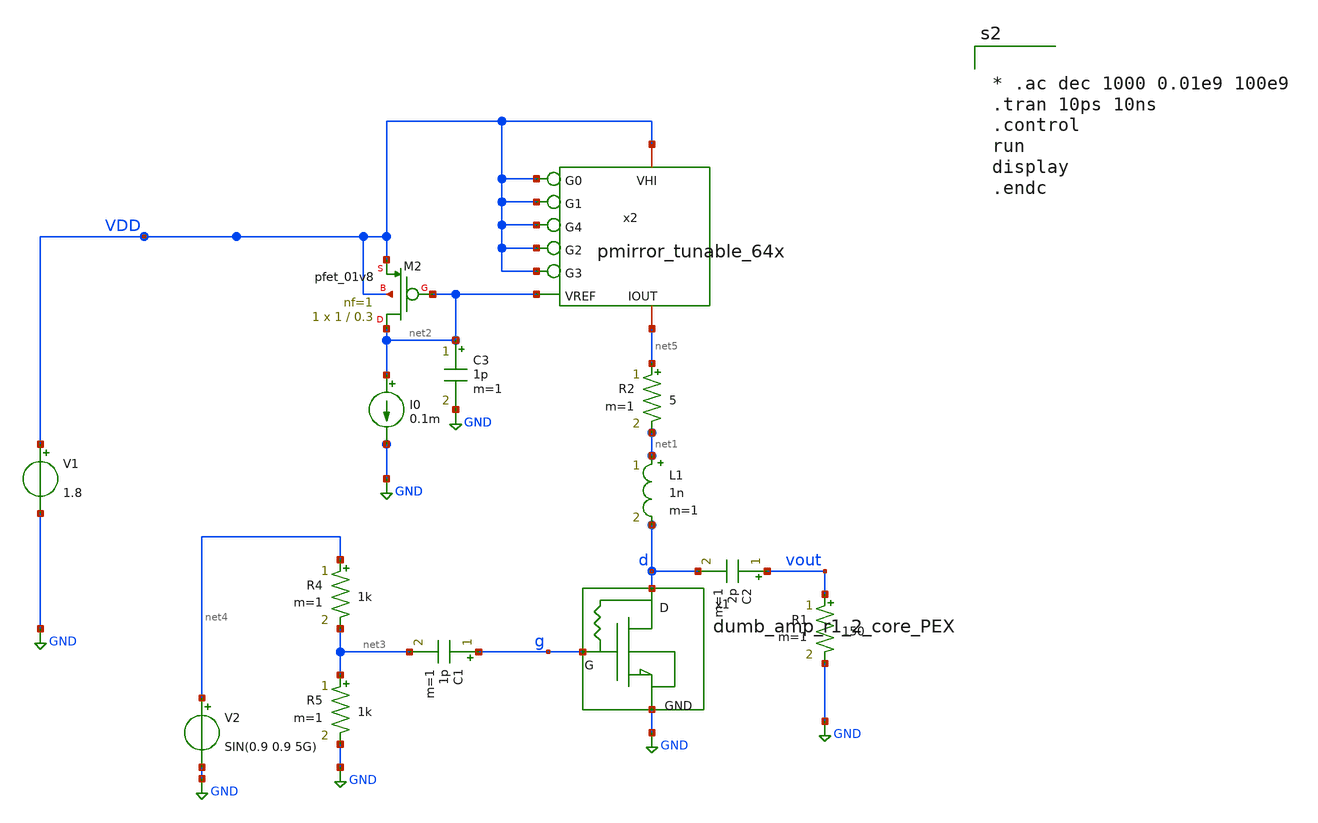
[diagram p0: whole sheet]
** sch_path: xschem/dumb_amp_r1_2_PEX_tran.sch
**.subckt dumb_amp_r1_2_PEX_tran
V1 VDD GND 1.8
V2 net4 GND SIN(0.9 0.9 5G)
C1 g net3 1p m=1
C2 vout d 2p m=1
L1 net1 d 1n m=1
R2 net5 net1 5 m=1
XM2 net2 net2 VDD VDD sky130_fd_pr__pfet_01v8 L=0.3 W=1 nf=1 ad='int((nf+1)/2) * W/nf * 0.29' as='int((nf+2)/2) * W/nf * 0.29'
+ pd='2*int((nf+1)/2) * (W/nf + 0.29)' ps='2*int((nf+2)/2) * (W/nf + 0.29)' nrd='0.29 / W' nrs='0.29 / W'
+ sa=0 sb=0 sd=0 mult=1 m=1
I0 net2 GND 0.1m
C3 net2 GND 1p m=1
R1 vout GND 150 m=1
R4 net4 net3 1k m=1
R5 net3 GND 1k m=1
x1 g d GND dumb_amp_r1_2_core_PEX
x2 VDD VDD VDD VDD VDD VDD net2 net5 pmirror_tunable_64x
**** begin user architecture code
.lib $::SKYWATER_MODELS/sky130.lib.spice tt
* .include $::PDKPATH/libs.ref/sky130_fd_sc_hvl/spice/sky130_fd_sc_hvl.spice



* .ac dec 1000 0.01e9 100e9
.tran 10ps 10ns
.control
run
display
.endc


**** end user architecture code
**.ends

* expanding   symbol:  dumb_amp_r1_2_core_PEX.sym # of pins=3
** sym_path: xschem/dumb_amp_r1_2_core_PEX.sym
** sch_path: xschem/dumb_amp_r1_2_core_PEX.sch
.subckt dumb_amp_r1_2_core_PEX G D GND
*.iopin G
*.iopin D
*.iopin GND
**** begin user architecture code

.subckt dumb_amp_core_pex NGATE NDRAIN VSUBS
.subckt sky130_fd_pr__rf_nfet_01v8_aM02W5p00L0p15 DRAIN GATE SOURCE SUBSTRATE
X0 DRAIN GATE SOURCE SUBSTRATE sky130_fd_pr__nfet_01v8 ad=1.414e+12p pd=1.066e+07u as=2.828e+12p
+ ps=2.132e+07u w=5.05e+06u l=150000u
X1 SOURCE GATE DRAIN SUBSTRATE sky130_fd_pr__nfet_01v8 ad=0p pd=0u as=0p ps=0u w=5.05e+06u l=150000u
C0 DRAIN SOURCE 3.59fF
C1 GATE SOURCE 0.46fF
C2 DRAIN GATE 0.34fF
C3 DRAIN SUBSTRATE 0.40fF
C4 SOURCE SUBSTRATE 2.44fF
C5 GATE SUBSTRATE 0.64fF
.ends
.subckt nfet_3x_2 D G S sub
Xsky130_fd_pr__rf_nfet_01v8_aM02W5p00L0p15_0 D G S sub sky130_fd_pr__rf_nfet_01v8_aM02W5p00L0p15
Xsky130_fd_pr__rf_nfet_01v8_aM02W5p00L0p15_1 D G S sub sky130_fd_pr__rf_nfet_01v8_aM02W5p00L0p15
Xsky130_fd_pr__rf_nfet_01v8_aM02W5p00L0p15_2 D G S sub sky130_fd_pr__rf_nfet_01v8_aM02W5p00L0p15
C0 G sub 1.34fF
C1 S D -0.11fF
C2 S G 2.13fF
C3 G D 1.69fF
C4 S sub -0.01fF
C5 D sub -0.05fF
C6 sub 0 -1.34fF
C7 D 0 0.62fF
C8 S 0 6.66fF
C9 G 0 1.96fF
.ends
.subckt RF_nfet_6xaM02W5p0L0p15 G S D B
Xnfet_3x_2_0 D G S B nfet_3x_2
Xnfet_3x_2_1 D G S B nfet_3x_2
C0 D B -0.02fF
C1 G S 0.20fF
C2 G B 0.06fF
C3 G D 0.14fF
C4 S B 0.02fF
C5 D S 0.01fF
C6 B 0 -3.73fF
C7 D 0 1.02fF
C8 S 0 13.03fF
C9 G 0 3.30fF
.ends
.subckt sky130_fd_pr__res_generic_po_JFYRVD a_75_284# a_n141_n357# a_n271_n487#
R0 a_n141_n357# a_75_284# sky130_fd_pr__res_generic_po w=330000u l=6.2e+06u
C0 a_n141_n357# a_n271_n487# 0.14fF
C1 a_75_284# a_n271_n487# 0.14fF
.ends
XRF_nfet_6xaM02W5p0L0p15_0 NGATE NDRAIN VSUBS VSUBS RF_nfet_6xaM02W5p0L0p15
Xsky130_fd_pr__res_generic_po_JFYRVD_0 NGATE NDRAIN VSUBS sky130_fd_pr__res_generic_po_JFYRVD
C0 VSUBS NDRAIN 1.42fF
C1 NGATE VSUBS 2.81fF
C2 NGATE NDRAIN 2.91fF
C5 NDRAIN VSUBS 14.22fF
C6 NGATE VSUBS 3.28fF
.ends

XDUT G D GND dumb_amp_core_pex


**** end user architecture code
.ends


* expanding   symbol:  pmirror_tunable_64x.sym # of pins=8
** sym_path: xschem/pmirror_tunable_64x.sym
** sch_path: xschem/pmirror_tunable_64x.sch
.subckt pmirror_tunable_64x VHI G0 G1 G4 G2 G3 VREF IOUT
*.ipin G0
*.ipin G1
*.ipin G2
*.ipin G3
*.ipin G4
*.ipin VREF
*.iopin VHI
*.iopin IOUT
XM3 IOUT net1 VHI VHI sky130_fd_pr__pfet_01v8 L=0.3 W=1 nf=1 ad='int((nf+1)/2) * W/nf * 0.29' as='int((nf+2)/2) * W/nf * 0.29'
+ pd='2*int((nf+1)/2) * (W/nf + 0.29)' ps='2*int((nf+2)/2) * (W/nf + 0.29)' nrd='0.29 / W' nrs='0.29 / W'
+ sa=0 sb=0 sd=0 mult=2 m=2
XM5 net1 net6 VHI VHI sky130_fd_pr__pfet_01v8 L=0.15 W=1 nf=1 ad='int((nf+1)/2) * W/nf * 0.29' as='int((nf+2)/2) * W/nf * 0.29'
+ pd='2*int((nf+1)/2) * (W/nf + 0.29)' ps='2*int((nf+2)/2) * (W/nf + 0.29)' nrd='0.29 / W' nrs='0.29 / W'
+ sa=0 sb=0 sd=0 mult=1 m=1
R3 net1 VREF 1k m=1
R1 net6 G0 1k m=1
XM1 IOUT net2 VHI VHI sky130_fd_pr__pfet_01v8 L=0.3 W=1 nf=1 ad='int((nf+1)/2) * W/nf * 0.29' as='int((nf+2)/2) * W/nf * 0.29'
+ pd='2*int((nf+1)/2) * (W/nf + 0.29)' ps='2*int((nf+2)/2) * (W/nf + 0.29)' nrd='0.29 / W' nrs='0.29 / W'
+ sa=0 sb=0 sd=0 mult=4 m=4
XM2 net2 net7 VHI VHI sky130_fd_pr__pfet_01v8 L=0.15 W=1 nf=1 ad='int((nf+1)/2) * W/nf * 0.29' as='int((nf+2)/2) * W/nf * 0.29'
+ pd='2*int((nf+1)/2) * (W/nf + 0.29)' ps='2*int((nf+2)/2) * (W/nf + 0.29)' nrd='0.29 / W' nrs='0.29 / W'
+ sa=0 sb=0 sd=0 mult=1 m=1
R2 net2 VREF 1k m=1
R4 net7 G1 1k m=1
XM4 IOUT net3 VHI VHI sky130_fd_pr__pfet_01v8 L=0.3 W=1 nf=1 ad='int((nf+1)/2) * W/nf * 0.29' as='int((nf+2)/2) * W/nf * 0.29'
+ pd='2*int((nf+1)/2) * (W/nf + 0.29)' ps='2*int((nf+2)/2) * (W/nf + 0.29)' nrd='0.29 / W' nrs='0.29 / W'
+ sa=0 sb=0 sd=0 mult=8 m=8
XM6 net3 net8 VHI VHI sky130_fd_pr__pfet_01v8 L=0.15 W=1 nf=1 ad='int((nf+1)/2) * W/nf * 0.29' as='int((nf+2)/2) * W/nf * 0.29'
+ pd='2*int((nf+1)/2) * (W/nf + 0.29)' ps='2*int((nf+2)/2) * (W/nf + 0.29)' nrd='0.29 / W' nrs='0.29 / W'
+ sa=0 sb=0 sd=0 mult=1 m=1
R5 net3 VREF 1k m=1
R6 net8 G2 1k m=1
XM7 IOUT net4 VHI VHI sky130_fd_pr__pfet_01v8 L=0.3 W=1 nf=1 ad='int((nf+1)/2) * W/nf * 0.29' as='int((nf+2)/2) * W/nf * 0.29'
+ pd='2*int((nf+1)/2) * (W/nf + 0.29)' ps='2*int((nf+2)/2) * (W/nf + 0.29)' nrd='0.29 / W' nrs='0.29 / W'
+ sa=0 sb=0 sd=0 mult=16 m=16
XM8 net4 net9 VHI VHI sky130_fd_pr__pfet_01v8 L=0.15 W=1 nf=1 ad='int((nf+1)/2) * W/nf * 0.29' as='int((nf+2)/2) * W/nf * 0.29'
+ pd='2*int((nf+1)/2) * (W/nf + 0.29)' ps='2*int((nf+2)/2) * (W/nf + 0.29)' nrd='0.29 / W' nrs='0.29 / W'
+ sa=0 sb=0 sd=0 mult=1 m=1
R7 net4 VREF 1k m=1
R8 net9 G3 1k m=1
XM9 IOUT net5 VHI VHI sky130_fd_pr__pfet_01v8 L=0.3 W=1 nf=1 ad='int((nf+1)/2) * W/nf * 0.29' as='int((nf+2)/2) * W/nf * 0.29'
+ pd='2*int((nf+1)/2) * (W/nf + 0.29)' ps='2*int((nf+2)/2) * (W/nf + 0.29)' nrd='0.29 / W' nrs='0.29 / W'
+ sa=0 sb=0 sd=0 mult=32 m=32
XM10 net5 net10 VHI VHI sky130_fd_pr__pfet_01v8 L=0.15 W=1 nf=1 ad='int((nf+1)/2) * W/nf * 0.29' as='int((nf+2)/2) * W/nf * 0.29'
+ pd='2*int((nf+1)/2) * (W/nf + 0.29)' ps='2*int((nf+2)/2) * (W/nf + 0.29)' nrd='0.29 / W' nrs='0.29 / W'
+ sa=0 sb=0 sd=0 mult=1 m=1
R9 net5 VREF 1k m=1
R10 net10 G4 1k m=1
.ends

.GLOBAL GND
.end
